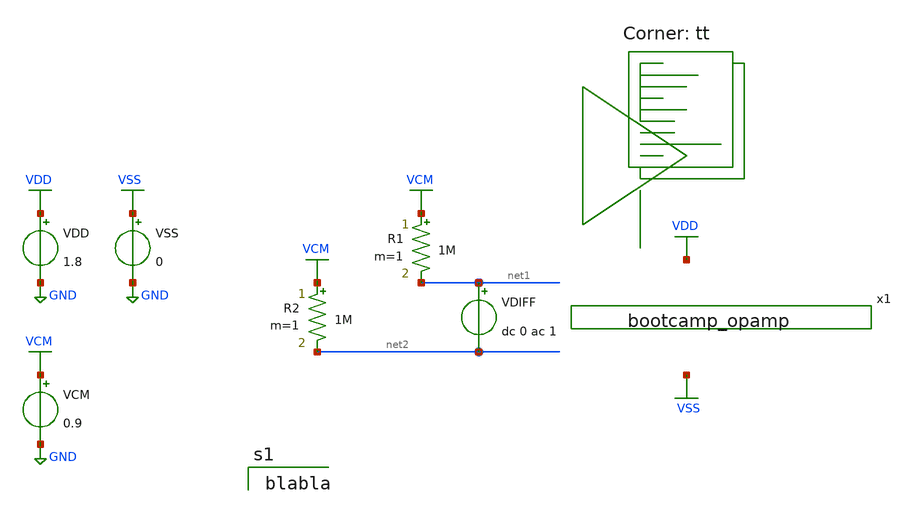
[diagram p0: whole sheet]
** sch_path: analog/build/schematic/tb_ac_analysis.sch
**.subckt tb_ac_analysis
x1 bootcamp_opamp
VDIFF net1 net2 dc 0 ac 1
R1 VCM net1 1M m=1
R2 VCM net2 1M m=1
VDD VDD GND 1.8
VCM VCM GND 0.9
VSS VSS GND 0
**** begin user architecture code

blabla

.lib $::SKYWATER_MODELS/sky130.lib.spice tt
**** end user architecture code
**.ends

* expanding   symbol:  bootcamp_opamp.sym # of pins=0
** sym_path: analog/schematics/bootcamp_opamp.sym
** sch_path: analog/schematics/bootcamp_opamp.sch
.subckt bootcamp_opamp
XM1 net1 net5 net3 net6 sky130_fd_pr__nfet_01v8 L=0.15 W=1 nf=1 ad='int((nf+1)/2) * W/nf * 0.29' as='int((nf+2)/2) * W/nf * 0.29'
+ pd='2*int((nf+1)/2) * (W/nf + 0.29)' ps='2*int((nf+2)/2) * (W/nf + 0.29)' nrd='0.29 / W' nrs='0.29 / W'
+ sa=0 sb=0 sd=0 mult=1 m=1
XM2 net2 net7 net3 net8 sky130_fd_pr__nfet_01v8 L=0.15 W=1 nf=1 ad='int((nf+1)/2) * W/nf * 0.29' as='int((nf+2)/2) * W/nf * 0.29'
+ pd='2*int((nf+1)/2) * (W/nf + 0.29)' ps='2*int((nf+2)/2) * (W/nf + 0.29)' nrd='0.29 / W' nrs='0.29 / W'
+ sa=0 sb=0 sd=0 mult=1 m=1
XM3 net1 net1 net4 net9 sky130_fd_pr__pfet_01v8 L=0.15 W=1 nf=1 ad='int((nf+1)/2) * W/nf * 0.29' as='int((nf+2)/2) * W/nf * 0.29'
+ pd='2*int((nf+1)/2) * (W/nf + 0.29)' ps='2*int((nf+2)/2) * (W/nf + 0.29)' nrd='0.29 / W' nrs='0.29 / W'
+ sa=0 sb=0 sd=0 mult=1 m=1
XM4 net2 net1 net4 net10 sky130_fd_pr__pfet_01v8 L=0.15 W=1 nf=1 ad='int((nf+1)/2) * W/nf * 0.29' as='int((nf+2)/2) * W/nf * 0.29'
+ pd='2*int((nf+1)/2) * (W/nf + 0.29)' ps='2*int((nf+2)/2) * (W/nf + 0.29)' nrd='0.29 / W' nrs='0.29 / W'
+ sa=0 sb=0 sd=0 mult=1 m=1
XM5 net3 net11 net12 net13 sky130_fd_pr__nfet_01v8 L=0.15 W=1 nf=1 ad='int((nf+1)/2) * W/nf * 0.29' as='int((nf+2)/2) * W/nf * 0.29'
+ pd='2*int((nf+1)/2) * (W/nf + 0.29)' ps='2*int((nf+2)/2) * (W/nf + 0.29)' nrd='0.29 / W' nrs='0.29 / W'
+ sa=0 sb=0 sd=0 mult=1 m=1
.ends

.GLOBAL GND
.GLOBAL VDD
.GLOBAL VCM
.GLOBAL VSS
.end
